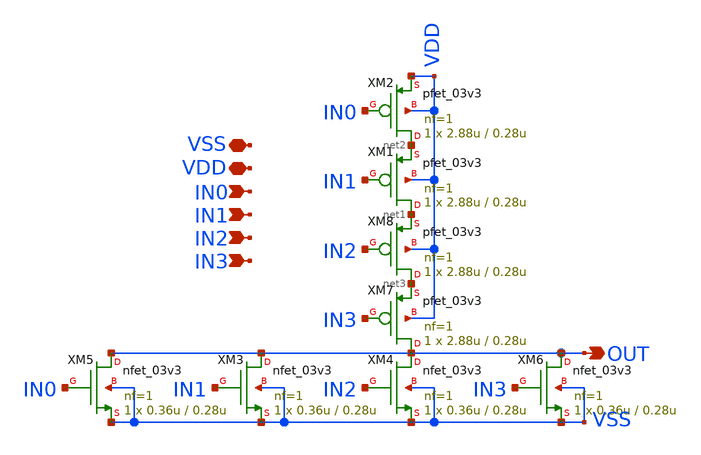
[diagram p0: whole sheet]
** sch_path: CAD4/nor4.sch
**.subckt nor4 VSS VDD IN0 IN1 OUT IN2 IN3
*.iopin VSS
*.iopin VDD
*.ipin IN0
*.ipin IN1
*.opin OUT
*.ipin IN2
*.ipin IN3
XM1 net1 IN1 net2 VDD pfet_03v3 L=0.28u W=2.88u nf=1 ad='int((nf+1)/2) * W/nf * 0.18u' as='int((nf+2)/2) * W/nf * 0.18u'
+ pd='2*int((nf+1)/2) * (W/nf + 0.18u)' ps='2*int((nf+2)/2) * (W/nf + 0.18u)' nrd='0.18u / W' nrs='0.18u / W'
+ sa=0 sb=0 sd=0 m=1
XM2 net2 IN0 VDD VDD pfet_03v3 L=0.28u W=2.88u nf=1 ad='int((nf+1)/2) * W/nf * 0.18u' as='int((nf+2)/2) * W/nf * 0.18u'
+ pd='2*int((nf+1)/2) * (W/nf + 0.18u)' ps='2*int((nf+2)/2) * (W/nf + 0.18u)' nrd='0.18u / W' nrs='0.18u / W'
+ sa=0 sb=0 sd=0 m=1
XM3 OUT IN1 VSS VSS nfet_03v3 L=0.28u W=0.36u nf=1 ad='int((nf+1)/2) * W/nf * 0.18u' as='int((nf+2)/2) * W/nf * 0.18u'
+ pd='2*int((nf+1)/2) * (W/nf + 0.18u)' ps='2*int((nf+2)/2) * (W/nf + 0.18u)' nrd='0.18u / W' nrs='0.18u / W'
+ sa=0 sb=0 sd=0 m=1
XM4 OUT IN2 VSS VSS nfet_03v3 L=0.28u W=0.36u nf=1 ad='int((nf+1)/2) * W/nf * 0.18u' as='int((nf+2)/2) * W/nf * 0.18u'
+ pd='2*int((nf+1)/2) * (W/nf + 0.18u)' ps='2*int((nf+2)/2) * (W/nf + 0.18u)' nrd='0.18u / W' nrs='0.18u / W'
+ sa=0 sb=0 sd=0 m=1
XM5 OUT IN0 VSS VSS nfet_03v3 L=0.28u W=0.36u nf=1 ad='int((nf+1)/2) * W/nf * 0.18u' as='int((nf+2)/2) * W/nf * 0.18u'
+ pd='2*int((nf+1)/2) * (W/nf + 0.18u)' ps='2*int((nf+2)/2) * (W/nf + 0.18u)' nrd='0.18u / W' nrs='0.18u / W'
+ sa=0 sb=0 sd=0 m=1
XM6 OUT IN3 VSS VSS nfet_03v3 L=0.28u W=0.36u nf=1 ad='int((nf+1)/2) * W/nf * 0.18u' as='int((nf+2)/2) * W/nf * 0.18u'
+ pd='2*int((nf+1)/2) * (W/nf + 0.18u)' ps='2*int((nf+2)/2) * (W/nf + 0.18u)' nrd='0.18u / W' nrs='0.18u / W'
+ sa=0 sb=0 sd=0 m=1
XM7 OUT IN3 net3 VDD pfet_03v3 L=0.28u W=2.88u nf=1 ad='int((nf+1)/2) * W/nf * 0.18u' as='int((nf+2)/2) * W/nf * 0.18u'
+ pd='2*int((nf+1)/2) * (W/nf + 0.18u)' ps='2*int((nf+2)/2) * (W/nf + 0.18u)' nrd='0.18u / W' nrs='0.18u / W'
+ sa=0 sb=0 sd=0 m=1
XM8 net3 IN2 net1 VDD pfet_03v3 L=0.28u W=2.88u nf=1 ad='int((nf+1)/2) * W/nf * 0.18u' as='int((nf+2)/2) * W/nf * 0.18u'
+ pd='2*int((nf+1)/2) * (W/nf + 0.18u)' ps='2*int((nf+2)/2) * (W/nf + 0.18u)' nrd='0.18u / W' nrs='0.18u / W'
+ sa=0 sb=0 sd=0 m=1
**.ends
.end
